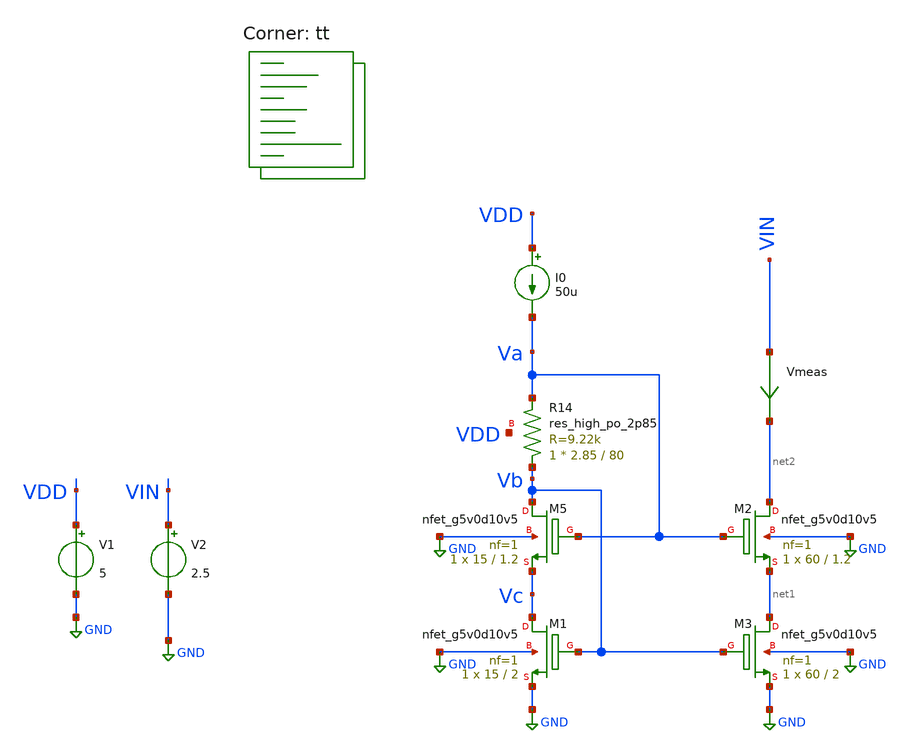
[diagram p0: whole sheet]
** sch_path: old stuff/my_amp_test/first stage/current_mirror_test.sch
**.subckt current_mirror_test
V1 VDD GND 5
V2 VIN GND 2.5
I0 VDD Va 50u
Vmeas VIN net2 0
.save i(vmeas)
XR14 Vb Va VDD sky130_fd_pr__res_high_po_2p85 L=80 mult=1 m=1
XM5 Vb Va Vc GND sky130_fd_pr__nfet_g5v0d10v5 L=1.2 W=15 nf=1 ad='int((1 + 1)/2) * 15 / 1 * 0.29' as='int((1 + 2)/2) * 15 / 1 * 0.29'
+ pd='2*int((1 + 1)/2) * (15 / 1 + 0.29)' ps='2*int((1 + 2)/2) * (15 / 1 + 0.29)' nrd='0.29 / 15 ' nrs='0.29 / 15 '
+ sa=0 sb=0 sd=0 mult=1 m=1
XM1 Vc Vb GND GND sky130_fd_pr__nfet_g5v0d10v5 L=2 W=15 nf=1 ad='int((1 + 1)/2) * 15 / 1 * 0.29' as='int((1 + 2)/2) * 15 / 1 * 0.29'
+ pd='2*int((1 + 1)/2) * (15 / 1 + 0.29)' ps='2*int((1 + 2)/2) * (15 / 1 + 0.29)' nrd='0.29 / 15 ' nrs='0.29 / 15 '
+ sa=0 sb=0 sd=0 mult=1 m=1
XM2 net2 Va net1 GND sky130_fd_pr__nfet_g5v0d10v5 L=1.2 W=60 nf=1 ad='int((1 + 1)/2) * 60 / 1 * 0.29'
+ as='int((1 + 2)/2) * 60 / 1 * 0.29' pd='2*int((1 + 1)/2) * (60 / 1 + 0.29)' ps='2*int((1 + 2)/2) * (60 / 1 + 0.29)'
+ nrd='0.29 / 60 ' nrs='0.29 / 60 ' sa=0 sb=0 sd=0 mult=1 m=1
XM3 net1 Vb GND GND sky130_fd_pr__nfet_g5v0d10v5 L=2 W=60 nf=1 ad='int((1 + 1)/2) * 60 / 1 * 0.29' as='int((1 + 2)/2) * 60 / 1 * 0.29'
+ pd='2*int((1 + 1)/2) * (60 / 1 + 0.29)' ps='2*int((1 + 2)/2) * (60 / 1 + 0.29)' nrd='0.29 / 60 ' nrs='0.29 / 60 '
+ sa=0 sb=0 sd=0 mult=1 m=1
**** begin user architecture code

**************************************************************
**************************************************************
**************************************************************
**************************************************************
**************************************************************
*LIBs*********************************************************
**************************************************************
**************************************************************
**************************************************************
**************************************************************
**************************************************************
*.lib $::SKYWATER_MODELS/sky130.lib.spice tt
* chose the corners in the corner file
* tt_mm for mismatch
* ss ff sf fs standart corners
* ll hh lh hl capacitor and resistors corners
* mc for total process variation including corners
**************************************************************
**************************************************************
**************************************************************
**************************************************************
**************************************************************
*Corners/montecarlo options***********************************
**************************************************************
**************************************************************
**************************************************************
**************************************************************
**************************************************************
.TEMP 27
**************************************************************
**************************************************************
**************************************************************
**************************************************************
*SIMULATION and Plots*****************************************
**************************************************************
**************************************************************
**************************************************************
**************************************************************
.control
save all
dc V2 0 5 0.001
*dc simulation
*ploting VIN VOUT and the voltage gain
plot i(Vmeas)
plot 1/deriv(i(Vmeas))
plot v(Va) v(Vb) v(Vc)
.endc

.lib $::SKYWATER_MODELS/sky130.lib.spice tt
**** end user architecture code
**.ends
.GLOBAL GND
.end
